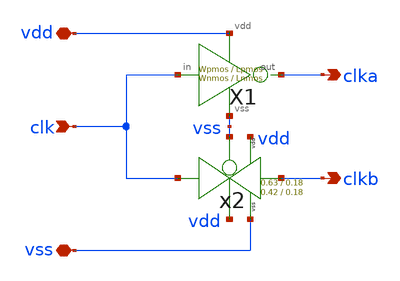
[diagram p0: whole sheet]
** sch_path: xschem/clkgen/comp_clks_1stage.sch
**.subckt comp_clks_1stage clk clka clkb vdd vss
*.ipin clk
*.opin clka
*.opin clkb
*.iopin vdd
*.iopin vss
X1 clk clka vdd vss inv Wpmos=Wpmos Lpmos=Lpmos Wnmos=Wnmos Lnmos=Lnmos
x2 clk clkb vss vdd vdd vss tg Wpmos=0.63 Lpmos=0.18 Wnmos=0.42 Lnmos=0.18
**.ends
.end
